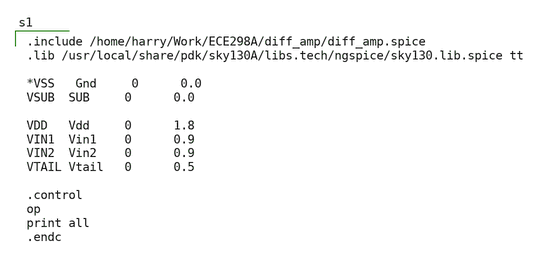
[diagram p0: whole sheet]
** sch_path: magic_xschem_ngspice/Magic_sim.sch
**.subckt Magic_sim
**** begin user architecture code

.include /home/harry/Work/ECE298A/diff_amp/diff_amp.spice
.lib /usr/local/share/pdk/sky130A/libs.tech/ngspice/sky130.lib.spice tt

*VSS   Gnd     0      0.0
VSUB  SUB     0      0.0

VDD   Vdd     0      1.8
VIN1  Vin1    0      0.9
VIN2  Vin2    0      0.9
VTAIL Vtail   0      0.5

.control
op
print all
.endc

**** end user architecture code
**.ends
.end
